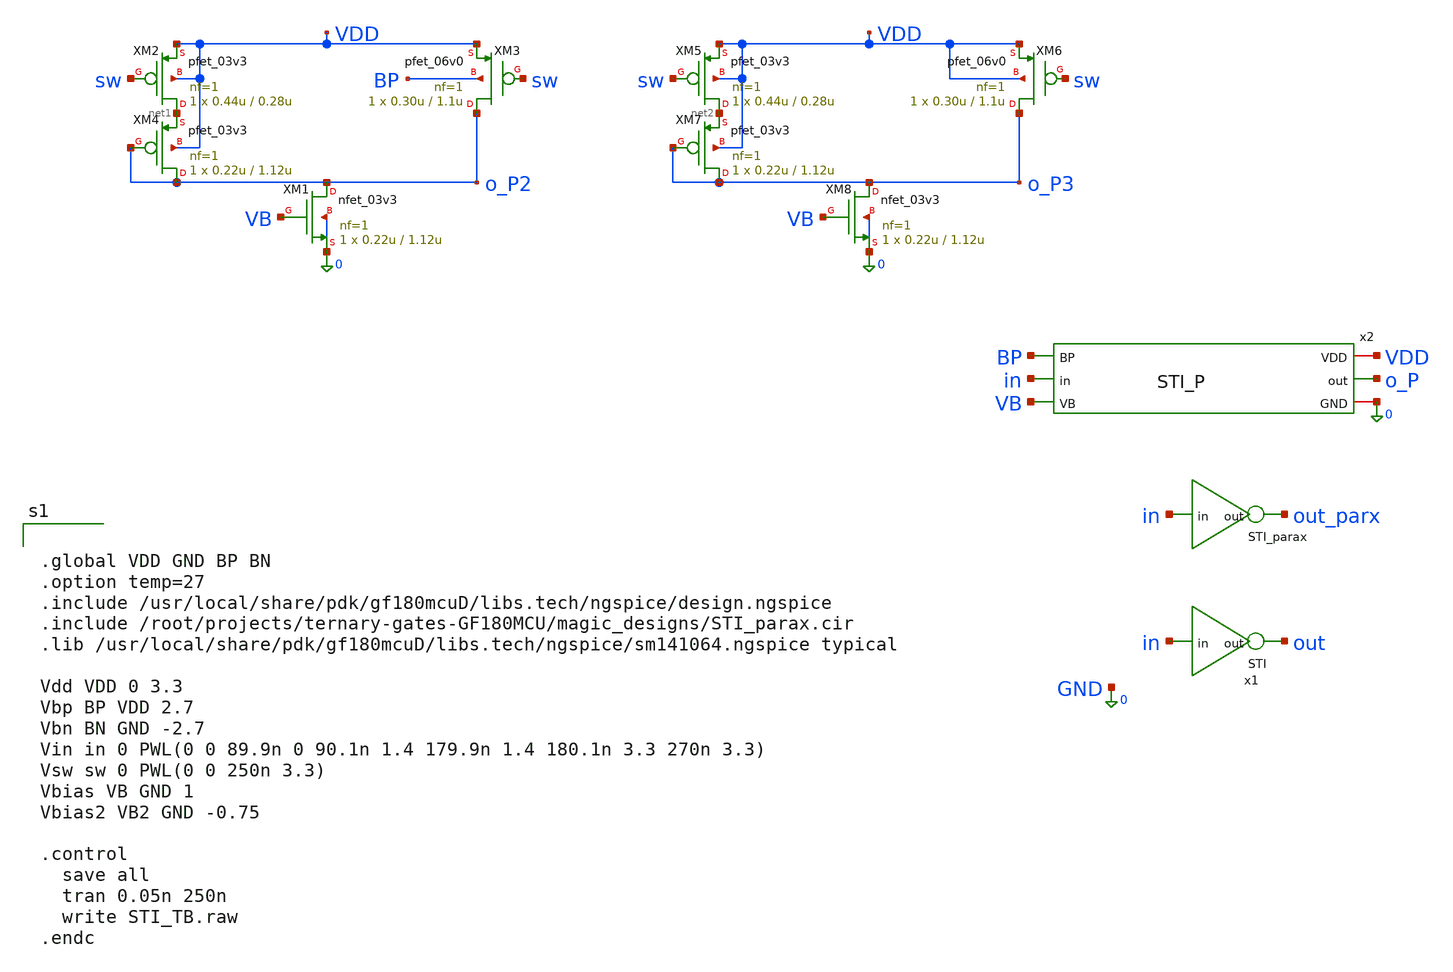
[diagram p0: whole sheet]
** sch_path: xschem_designs/STI_TB.sch
**.subckt STI_TB
x1 out_parx in STI_parax
x1 out in STI
x2 VDD BP in o_P VB 0 STI_P
XM2 net1 sw VDD VDD pfet_03v3 L=0.28u W=0.44u nf=1 ad='int((nf+1)/2) * W/nf * 0.18u' as='int((nf+2)/2) * W/nf * 0.18u'
+ pd='2*int((nf+1)/2) * (W/nf + 0.18u)' ps='2*int((nf+2)/2) * (W/nf + 0.18u)' nrd='0.18u / W' nrs='0.18u / W'
+ sa=0 sb=0 sd=0 m=1 par=1
XM3 o_P2 sw VDD BP pfet_06v0 L=1.1u W=0.30u nf=1 ad='int((nf+1)/2) * W/nf * 0.18u' as='int((nf+2)/2) * W/nf * 0.18u'
+ pd='2*int((nf+1)/2) * (W/nf + 0.18u)' ps='2*int((nf+2)/2) * (W/nf + 0.18u)' nrd='0.18u / W' nrs='0.18u / W'
+ sa=0 sb=0 sd=0 m=1
XM4 o_P2 o_P2 net1 VDD pfet_03v3 L=1.12u W=0.22u nf=1 ad='int((nf+1)/2) * W/nf * 0.18u' as='int((nf+2)/2) * W/nf * 0.18u'
+ pd='2*int((nf+1)/2) * (W/nf + 0.18u)' ps='2*int((nf+2)/2) * (W/nf + 0.18u)' nrd='0.18u / W' nrs='0.18u / W'
+ sa=0 sb=0 sd=0 m=1 par=1
XM5 net2 sw VDD VDD pfet_03v3 L=0.28u W=0.44u nf=1 ad='int((nf+1)/2) * W/nf * 0.18u' as='int((nf+2)/2) * W/nf * 0.18u'
+ pd='2*int((nf+1)/2) * (W/nf + 0.18u)' ps='2*int((nf+2)/2) * (W/nf + 0.18u)' nrd='0.18u / W' nrs='0.18u / W'
+ sa=0 sb=0 sd=0 m=1 par=1
XM6 o_P3 sw VDD VDD pfet_06v0 L=1.1u W=0.30u nf=1 ad='int((nf+1)/2) * W/nf * 0.18u' as='int((nf+2)/2) * W/nf * 0.18u'
+ pd='2*int((nf+1)/2) * (W/nf + 0.18u)' ps='2*int((nf+2)/2) * (W/nf + 0.18u)' nrd='0.18u / W' nrs='0.18u / W'
+ sa=0 sb=0 sd=0 m=1
XM7 o_P3 o_P3 net2 VDD pfet_03v3 L=1.12u W=0.22u nf=1 ad='int((nf+1)/2) * W/nf * 0.18u' as='int((nf+2)/2) * W/nf * 0.18u'
+ pd='2*int((nf+1)/2) * (W/nf + 0.18u)' ps='2*int((nf+2)/2) * (W/nf + 0.18u)' nrd='0.18u / W' nrs='0.18u / W'
+ sa=0 sb=0 sd=0 m=1 par=1
XM1 o_P2 VB 0 0 nfet_03v3 L=1.12u W=0.22u nf=1 ad='int((nf+1)/2) * W/nf * 0.18u' as='int((nf+2)/2) * W/nf * 0.18u'
+ pd='2*int((nf+1)/2) * (W/nf + 0.18u)' ps='2*int((nf+2)/2) * (W/nf + 0.18u)' nrd='0.18u / W' nrs='0.18u / W'
+ sa=0 sb=0 sd=0 m=1 par=1
XM8 o_P3 VB 0 0 nfet_03v3 L=1.12u W=0.22u nf=1 ad='int((nf+1)/2) * W/nf * 0.18u' as='int((nf+2)/2) * W/nf * 0.18u'
+ pd='2*int((nf+1)/2) * (W/nf + 0.18u)' ps='2*int((nf+2)/2) * (W/nf + 0.18u)' nrd='0.18u / W' nrs='0.18u / W'
+ sa=0 sb=0 sd=0 m=1 par=1
**** begin user architecture code


.global VDD GND BP BN
.option temp=27
.include /usr/local/share/pdk/gf180mcuD/libs.tech/ngspice/design.ngspice
.include /root/projects/ternary-gates-GF180MCU/magic_designs/STI_parax.cir
.lib /usr/local/share/pdk/gf180mcuD/libs.tech/ngspice/sm141064.ngspice typical

Vdd VDD 0 3.3
Vbp BP VDD 2.7
Vbn BN GND -2.7
Vin in 0 PWL(0 0 89.9n 0 90.1n 1.4 179.9n 1.4 180.1n 3.3 270n 3.3)
Vsw sw 0 PWL(0 0 250n 3.3)
Vbias VB GND 1
Vbias2 VB2 GND -0.75

.control
  save all
  tran 0.05n 250n
  write STI_TB.raw
.endc


**** end user architecture code
**.ends
.end
